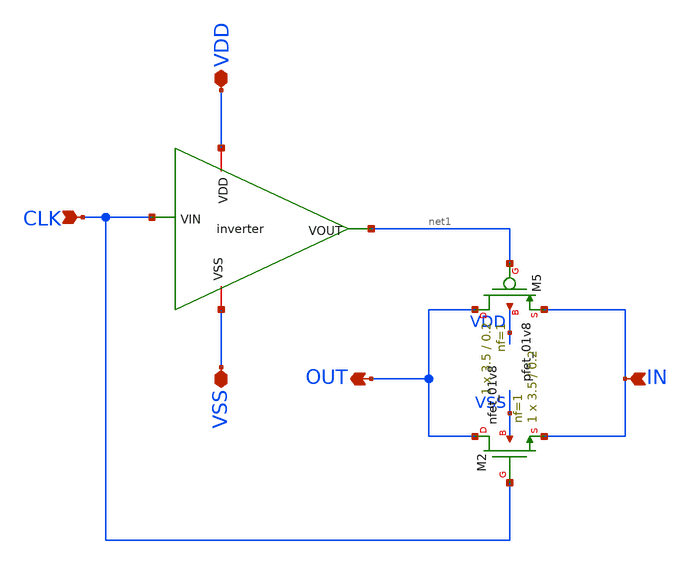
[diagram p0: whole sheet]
** sch_path: Xschem/PLL_TOP_Schematics/tg.sch
* Xschem/PLL_TOP_Schematics/inverter.sch:
* Copyright 2022 GlobalFoundries PDK Authors
* Licensed under the Apache License, Version 2.0 (the "License");
**.subckt tg VDD VSS CLK IN OUT
*.iopin VDD
*.iopin VSS
*.ipin CLK
*.ipin IN
*.opin OUT
x1 VDD CLK net1 VSS inverter
XM5 OUT net1 IN VDD sky130_fd_pr__pfet_01v8 L=0.2 W=3.5 nf=1 ad='int((nf+1)/2) * W/nf * 0.29' as='int((nf+2)/2) * W/nf * 0.29'
+ pd='2*int((nf+1)/2) * (W/nf + 0.29)' ps='2*int((nf+2)/2) * (W/nf + 0.29)' nrd='0.29 / W' nrs='0.29 / W'
+ sa=0 sb=0 sd=0 mult=1 m=1
XM2 OUT CLK IN VSS sky130_fd_pr__nfet_01v8 L=0.2 W=3.5 nf=1 ad='int((nf+1)/2) * W/nf * 0.29' as='int((nf+2)/2) * W/nf * 0.29'
+ pd='2*int((nf+1)/2) * (W/nf + 0.29)' ps='2*int((nf+2)/2) * (W/nf + 0.29)' nrd='0.29 / W' nrs='0.29 / W'
+ sa=0 sb=0 sd=0 mult=1 m=1
**.ends

* expanding   symbol:  inverter.sym # of pins=4
** sym_path: Xschem/PLL_TOP_Schematics/inverter.sym
** sch_path: Xschem/PLL_TOP_Schematics/inverter.sch
.subckt inverter VDD VIN VOUT VSS
*.iopin VDD
*.ipin VIN
*.opin VOUT
*.iopin VSS
XM5 VOUT VIN VDD VDD sky130_fd_pr__pfet_01v8 L=0.2 W=5 nf=1 ad='int((nf+1)/2) * W/nf * 0.29' as='int((nf+2)/2) * W/nf * 0.29'
+ pd='2*int((nf+1)/2) * (W/nf + 0.29)' ps='2*int((nf+2)/2) * (W/nf + 0.29)' nrd='0.29 / W' nrs='0.29 / W'
+ sa=0 sb=0 sd=0 mult=1 m=1
XM1 VOUT VIN VSS VSS sky130_fd_pr__nfet_01v8 L=0.2 W=2.5 nf=1 ad='int((nf+1)/2) * W/nf * 0.29' as='int((nf+2)/2) * W/nf * 0.29'
+ pd='2*int((nf+1)/2) * (W/nf + 0.29)' ps='2*int((nf+2)/2) * (W/nf + 0.29)' nrd='0.29 / W' nrs='0.29 / W'
+ sa=0 sb=0 sd=0 mult=1 m=1
.ends

.end
